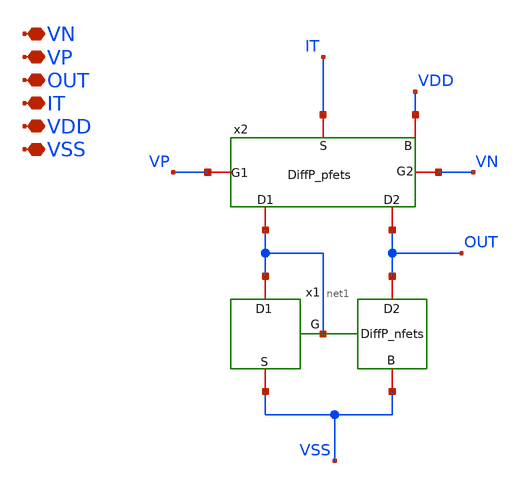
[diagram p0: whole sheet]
** sch_path: TIA_Filter/PseudoResistor/DiffP_net.sch
**.subckt DiffP_net VN VP OUT IT VDD VSS
*.iopin VN
*.iopin VP
*.iopin OUT
*.iopin IT
*.iopin VDD
*.iopin VSS
x1 net1 OUT net1 VSS VSS DiffP_nfets
x2 net1 OUT VP VN IT VDD DiffP_pfets
**.ends
.end
